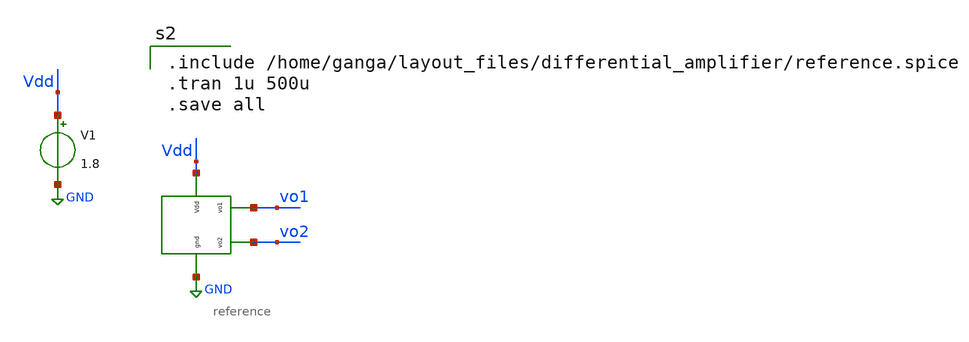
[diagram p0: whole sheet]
** sch_path: xschem/charge_pumps2/ref_postlayout.sch
**.subckt ref_postlayout
x1 Vdd GND vo1 vo2 reference
V1 Vdd GND 1.8
**** begin user architecture code

.include /home/ganga/layout_files/differential_amplifier/reference.spice
.tran 1u 500u
.save all


** opencircuitdesign pdks install
.lib $::SKYWATER_MODELS/sky130.lib.spice tt


**** end user architecture code
**.ends
.GLOBAL GND
.end
